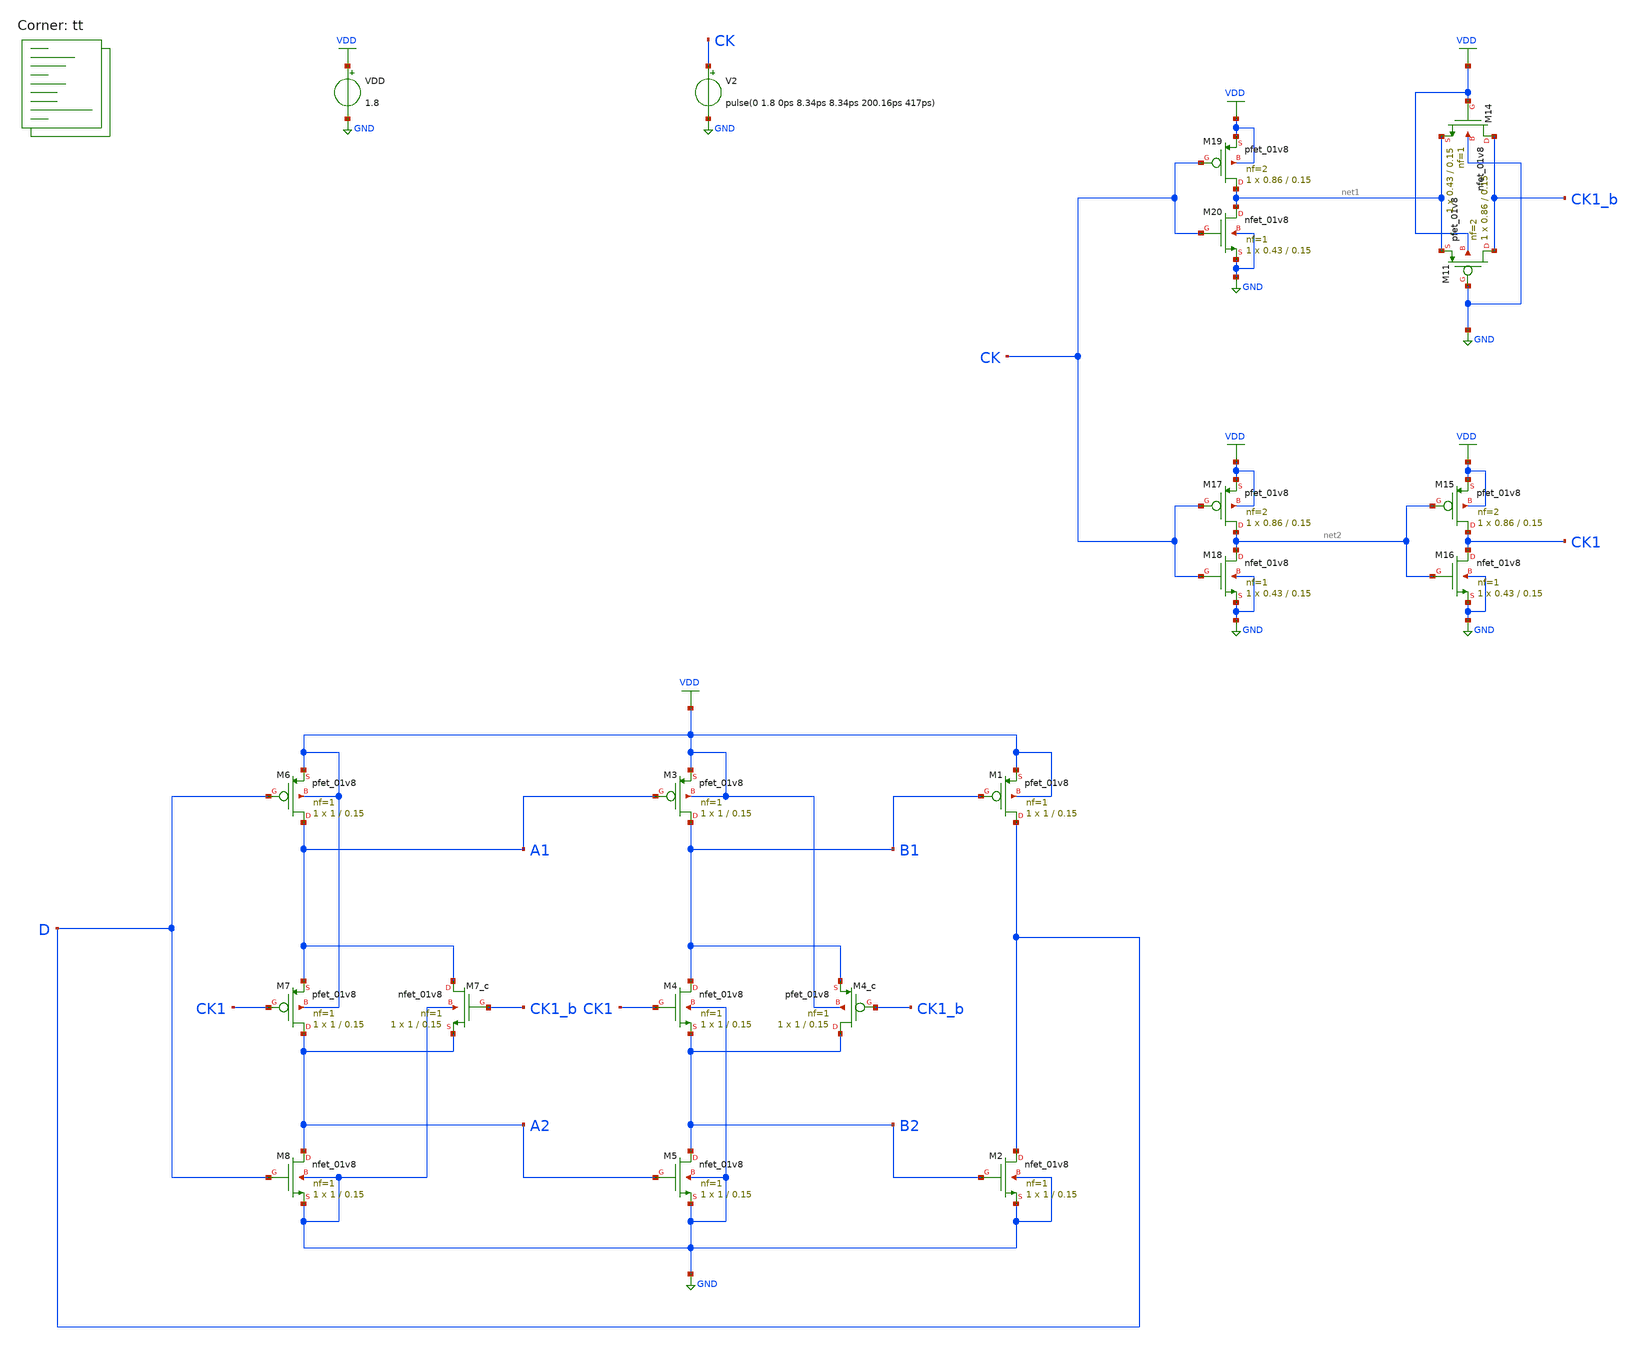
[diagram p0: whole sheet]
** sch_path: projects/pll/divider/xschem_ngspice/tb_TSPC_FF_comp_sw_divide2.sch
**.subckt tb_TSPC_FF_comp_sw_divide2
VDD VDD GND 1.8
XM1 D B1 VDD VDD sky130_fd_pr__pfet_01v8 L=0.15 W=1 nf=1 ad='int((nf+1)/2) * W/nf * 0.29' as='int((nf+2)/2) * W/nf * 0.29'
+ pd='2*int((nf+1)/2) * (W/nf + 0.29)' ps='2*int((nf+2)/2) * (W/nf + 0.29)' nrd='0.29 / W' nrs='0.29 / W'
+ sa=0 sb=0 sd=0 mult=1 m=1
XM4 B1 CK1 B2 GND sky130_fd_pr__nfet_01v8 L=0.15 W=1 nf=1 ad='int((nf+1)/2) * W/nf * 0.29' as='int((nf+2)/2) * W/nf * 0.29'
+ pd='2*int((nf+1)/2) * (W/nf + 0.29)' ps='2*int((nf+2)/2) * (W/nf + 0.29)' nrd='0.29 / W' nrs='0.29 / W'
+ sa=0 sb=0 sd=0 mult=1 m=1
XM2 D B2 GND GND sky130_fd_pr__nfet_01v8 L=0.15 W=1 nf=1 ad='int((nf+1)/2) * W/nf * 0.29' as='int((nf+2)/2) * W/nf * 0.29'
+ pd='2*int((nf+1)/2) * (W/nf + 0.29)' ps='2*int((nf+2)/2) * (W/nf + 0.29)' nrd='0.29 / W' nrs='0.29 / W'
+ sa=0 sb=0 sd=0 mult=1 m=1
XM3 B1 A1 VDD VDD sky130_fd_pr__pfet_01v8 L=0.15 W=1 nf=1 ad='int((nf+1)/2) * W/nf * 0.29' as='int((nf+2)/2) * W/nf * 0.29'
+ pd='2*int((nf+1)/2) * (W/nf + 0.29)' ps='2*int((nf+2)/2) * (W/nf + 0.29)' nrd='0.29 / W' nrs='0.29 / W'
+ sa=0 sb=0 sd=0 mult=1 m=1
XM5 B2 A2 GND GND sky130_fd_pr__nfet_01v8 L=0.15 W=1 nf=1 ad='int((nf+1)/2) * W/nf * 0.29' as='int((nf+2)/2) * W/nf * 0.29'
+ pd='2*int((nf+1)/2) * (W/nf + 0.29)' ps='2*int((nf+2)/2) * (W/nf + 0.29)' nrd='0.29 / W' nrs='0.29 / W'
+ sa=0 sb=0 sd=0 mult=1 m=1
XM6 A1 D VDD VDD sky130_fd_pr__pfet_01v8 L=0.15 W=1 nf=1 ad='int((nf+1)/2) * W/nf * 0.29' as='int((nf+2)/2) * W/nf * 0.29'
+ pd='2*int((nf+1)/2) * (W/nf + 0.29)' ps='2*int((nf+2)/2) * (W/nf + 0.29)' nrd='0.29 / W' nrs='0.29 / W'
+ sa=0 sb=0 sd=0 mult=1 m=1
XM8 A2 D GND GND sky130_fd_pr__nfet_01v8 L=0.15 W=1 nf=1 ad='int((nf+1)/2) * W/nf * 0.29' as='int((nf+2)/2) * W/nf * 0.29'
+ pd='2*int((nf+1)/2) * (W/nf + 0.29)' ps='2*int((nf+2)/2) * (W/nf + 0.29)' nrd='0.29 / W' nrs='0.29 / W'
+ sa=0 sb=0 sd=0 mult=1 m=1
XM7 A2 CK1 A1 VDD sky130_fd_pr__pfet_01v8 L=0.15 W=1 nf=1 ad='int((nf+1)/2) * W/nf * 0.29' as='int((nf+2)/2) * W/nf * 0.29'
+ pd='2*int((nf+1)/2) * (W/nf + 0.29)' ps='2*int((nf+2)/2) * (W/nf + 0.29)' nrd='0.29 / W' nrs='0.29 / W'
+ sa=0 sb=0 sd=0 mult=1 m=1
XM4_c B2 CK1_b B1 VDD sky130_fd_pr__pfet_01v8 L=0.15 W=1 nf=1 ad='int((nf+1)/2) * W/nf * 0.29' as='int((nf+2)/2) * W/nf * 0.29'
+ pd='2*int((nf+1)/2) * (W/nf + 0.29)' ps='2*int((nf+2)/2) * (W/nf + 0.29)' nrd='0.29 / W' nrs='0.29 / W'
+ sa=0 sb=0 sd=0 mult=1 m=1
XM7_c A1 CK1_b A2 GND sky130_fd_pr__nfet_01v8 L=0.15 W=1 nf=1 ad='int((nf+1)/2) * W/nf * 0.29' as='int((nf+2)/2) * W/nf * 0.29'
+ pd='2*int((nf+1)/2) * (W/nf + 0.29)' ps='2*int((nf+2)/2) * (W/nf + 0.29)' nrd='0.29 / W' nrs='0.29 / W'
+ sa=0 sb=0 sd=0 mult=1 m=1
V2 CK GND pulse(0 1.8 0ps 8.34ps 8.34ps 200.16ps 417ps)
XM11 CK1_b GND net1 VDD sky130_fd_pr__pfet_01v8 L=0.15 W=0.86 nf=2 ad='int((nf+1)/2) * W/nf * 0.29' as='int((nf+2)/2) * W/nf * 0.29'
+ pd='2*int((nf+1)/2) * (W/nf + 0.29)' ps='2*int((nf+2)/2) * (W/nf + 0.29)' nrd='0.29 / W' nrs='0.29 / W'
+ sa=0 sb=0 sd=0 mult=1 m=1
XM14 CK1_b VDD net1 GND sky130_fd_pr__nfet_01v8 L=0.15 W=0.43 nf=1 ad='int((nf+1)/2) * W/nf * 0.29' as='int((nf+2)/2) * W/nf * 0.29'
+ pd='2*int((nf+1)/2) * (W/nf + 0.29)' ps='2*int((nf+2)/2) * (W/nf + 0.29)' nrd='0.29 / W' nrs='0.29 / W'
+ sa=0 sb=0 sd=0 mult=1 m=1
XM15 CK1 net2 VDD VDD sky130_fd_pr__pfet_01v8 L=0.15 W=0.86 nf=2 ad='int((nf+1)/2) * W/nf * 0.29' as='int((nf+2)/2) * W/nf * 0.29'
+ pd='2*int((nf+1)/2) * (W/nf + 0.29)' ps='2*int((nf+2)/2) * (W/nf + 0.29)' nrd='0.29 / W' nrs='0.29 / W'
+ sa=0 sb=0 sd=0 mult=1 m=1
XM16 CK1 net2 GND GND sky130_fd_pr__nfet_01v8 L=0.15 W=0.43 nf=1 ad='int((nf+1)/2) * W/nf * 0.29' as='int((nf+2)/2) * W/nf * 0.29'
+ pd='2*int((nf+1)/2) * (W/nf + 0.29)' ps='2*int((nf+2)/2) * (W/nf + 0.29)' nrd='0.29 / W' nrs='0.29 / W'
+ sa=0 sb=0 sd=0 mult=1 m=1
XM17 net2 CK VDD VDD sky130_fd_pr__pfet_01v8 L=0.15 W=0.86 nf=2 ad='int((nf+1)/2) * W/nf * 0.29' as='int((nf+2)/2) * W/nf * 0.29'
+ pd='2*int((nf+1)/2) * (W/nf + 0.29)' ps='2*int((nf+2)/2) * (W/nf + 0.29)' nrd='0.29 / W' nrs='0.29 / W'
+ sa=0 sb=0 sd=0 mult=1 m=1
XM18 net2 CK GND GND sky130_fd_pr__nfet_01v8 L=0.15 W=0.43 nf=1 ad='int((nf+1)/2) * W/nf * 0.29' as='int((nf+2)/2) * W/nf * 0.29'
+ pd='2*int((nf+1)/2) * (W/nf + 0.29)' ps='2*int((nf+2)/2) * (W/nf + 0.29)' nrd='0.29 / W' nrs='0.29 / W'
+ sa=0 sb=0 sd=0 mult=1 m=1
XM19 net1 CK VDD VDD sky130_fd_pr__pfet_01v8 L=0.15 W=0.86 nf=2 ad='int((nf+1)/2) * W/nf * 0.29' as='int((nf+2)/2) * W/nf * 0.29'
+ pd='2*int((nf+1)/2) * (W/nf + 0.29)' ps='2*int((nf+2)/2) * (W/nf + 0.29)' nrd='0.29 / W' nrs='0.29 / W'
+ sa=0 sb=0 sd=0 mult=1 m=1
XM20 net1 CK GND GND sky130_fd_pr__nfet_01v8 L=0.15 W=0.43 nf=1 ad='int((nf+1)/2) * W/nf * 0.29' as='int((nf+2)/2) * W/nf * 0.29'
+ pd='2*int((nf+1)/2) * (W/nf + 0.29)' ps='2*int((nf+2)/2) * (W/nf + 0.29)' nrd='0.29 / W' nrs='0.29 / W'
+ sa=0 sb=0 sd=0 mult=1 m=1
**** begin user architecture code



.include /foss/pdks/sky130A/libs.ref/sky130_fd_sc_hd/spice/sky130_fd_sc_hd.spice

.option method=gear
.option wnflag=1
.option savecurrents

.save @m.xm1.msky130_fd_pr__pfet_01v8[gm] @m.xm2.msky130_fd_pr__nfet_01v8[gm] @m.xm3.msky130_fd_pr__pfet_01v8[gm] @m.xm4.msky130_fd_pr__nfet_01v8[gm] @m.xm4_c.msky130_fd_pr__pfet_01v8[gm] @m.xm5.msky130_fd_pr__nfet_01v8[gm] @m.xm6.msky130_fd_pr__pfet_01v8[gm] @m.xm7.msky130_fd_pr__pfet_01v8[gm] @m.xm7_c.msky130_fd_pr__nfet_01v8[gm] @m.xm8.msky130_fd_pr__nfet_01v8[gm]

*.ic v(d)=0
*.ic v(q)=0
*.ic v(q1)=0

.control

  save v(d) v(q1) v(q2) v(q1_b) v(q2_b) v(q3) v(a1) v(a2) v(a3) v(a4) v(b1) v(b2) v(b3) v(b4) v(ck)
+ v(ck1) v(ck1_b)
  * save all
  * tran 0.1n 1u
  tran 1p 20n

  remzerovec
  write tb_TSPC_FF_comp_sw_divide2.raw
  * set appendwrite

.endc



.lib $::SKYWATER_MODELS/sky130.lib.spice tt
**** end user architecture code
**.ends
.GLOBAL GND
.GLOBAL VDD
.end
